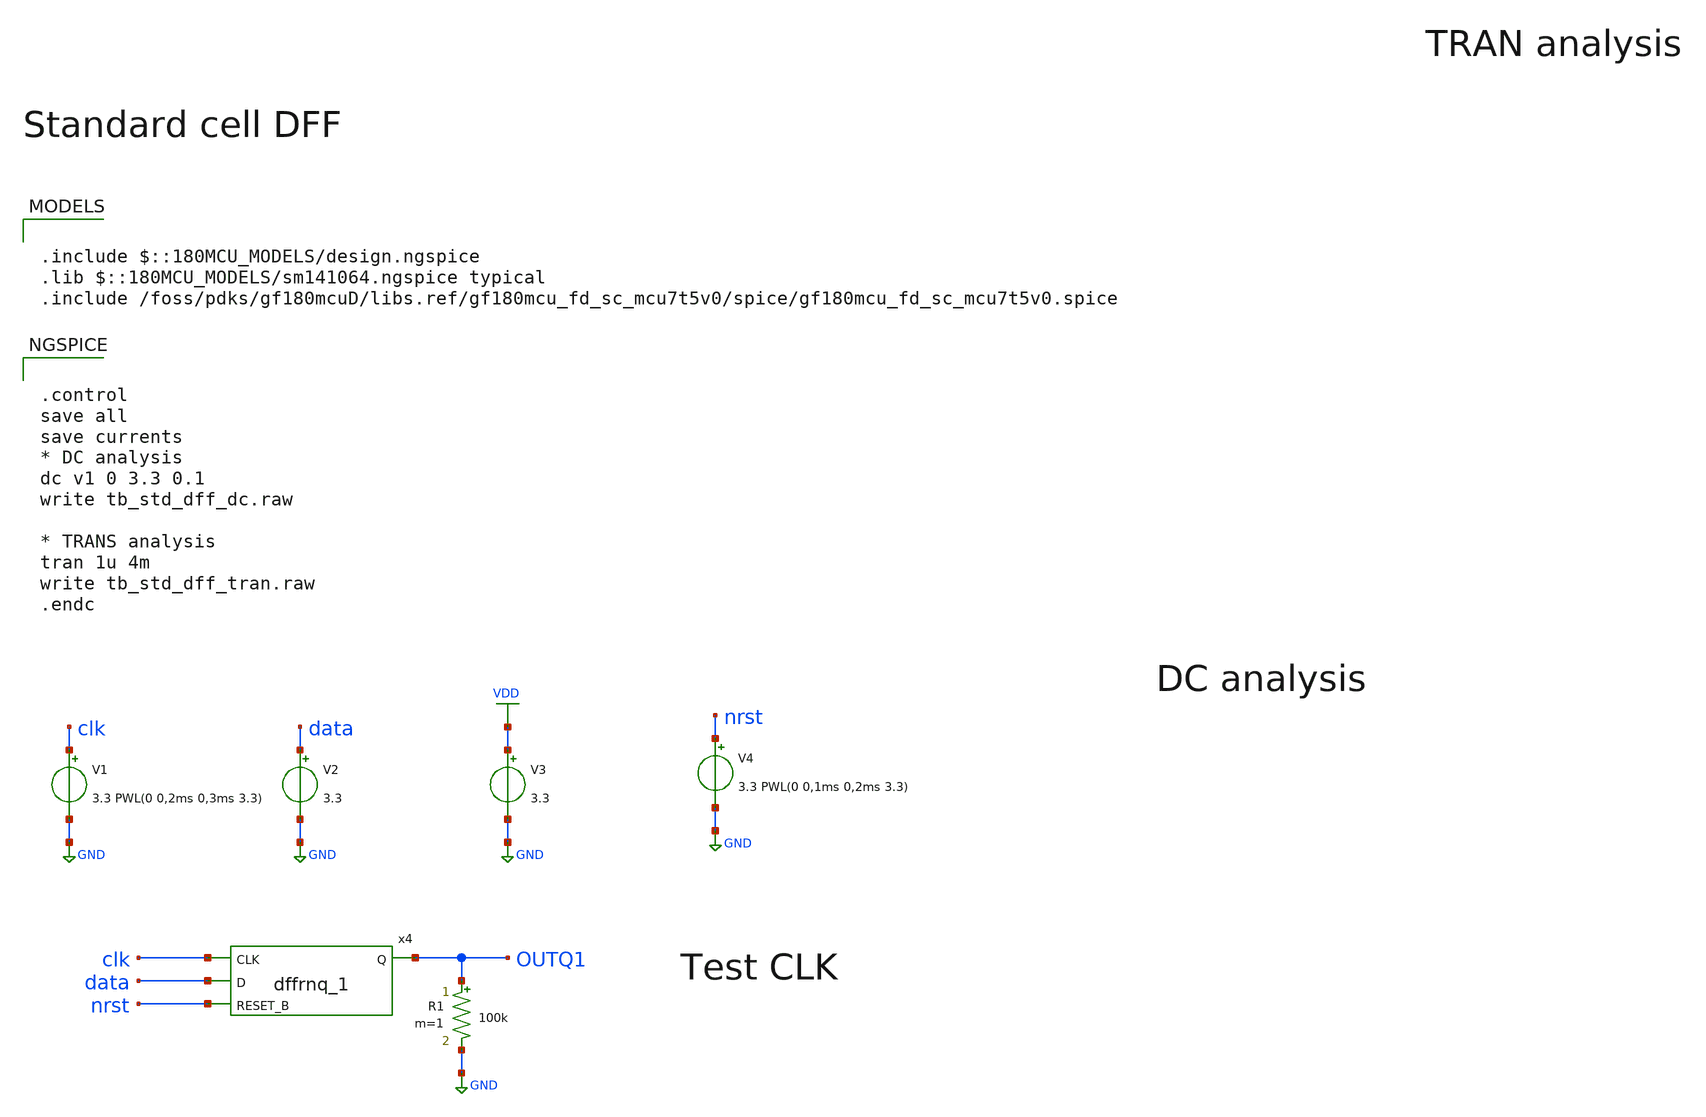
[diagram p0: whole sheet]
** sch_path: designs/libs/tb_analog/tb_std_dff/tb_std_dff.sch
* Copyright 2022 GlobalFoundries PDK Authors
* Licensed under the Apache License, Version 2.0 (the "License");
* you may not use this file except in compliance with the License.
* You may obtain a copy of the License at
* https://www.apache.org/licenses/LICENSE-2.0
* Unless required by applicable law or agreed to in writing, software
* distributed under the License is distributed on an "AS IS" BASIS,
* WITHOUT WARRANTIES OR CONDITIONS OF ANY KIND, either express or implied.
* See the License for the specific language governing permissions and
* limitations under the License.
**.subckt tb_std_dff
V1 clk GND 3.3 PWL(0 0,2ms 0,3ms 3.3)
V2 data GND 3.3
V3 VDD GND 3.3
R1 OUTQ1 GND 100k m=1
x4 data nrst clk OUTQ1 VDD VDD GND GND gf180mcu_fd_sc_mcu7t5v0__dffrnq_1
V4 nrst GND 3.3 PWL(0 0,1ms 0,2ms 3.3)
**** begin user architecture code

.include $::180MCU_MODELS/design.ngspice
.lib $::180MCU_MODELS/sm141064.ngspice typical
.include /foss/pdks/gf180mcuD/libs.ref/gf180mcu_fd_sc_mcu7t5v0/spice/gf180mcu_fd_sc_mcu7t5v0.spice




.control
save all
save currents
* DC analysis
dc v1 0 3.3 0.1
write tb_std_dff_dc.raw

* TRANS analysis
tran 1u 4m
write tb_std_dff_tran.raw
.endc


**** end user architecture code
**.ends
.GLOBAL VDD
.GLOBAL GND
.end
